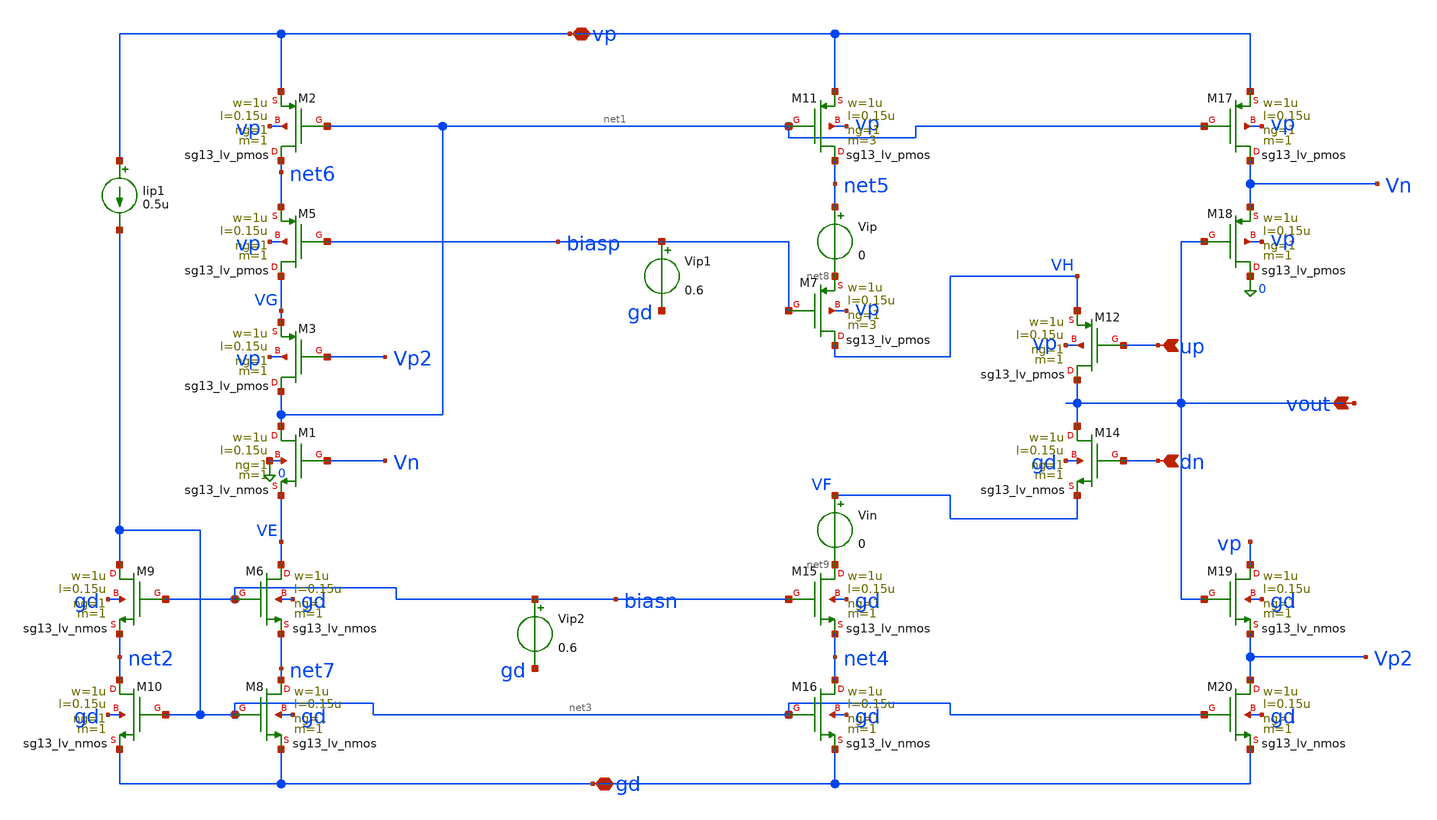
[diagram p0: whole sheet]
** sch_path: schematics/charge_pump/cp_v1_low_curr.sch
**.subckt cp_v1_low_curr up dn vp gd vout
*.ipin up
*.ipin dn
*.iopin vp
*.iopin gd
*.opin vout
XM7 VH biasp net8 vp sg13_lv_pmos w=1u l=0.15u ng=1 m=3 mm_ok=1
XM12 vout up VH vp sg13_lv_pmos w=1u l=0.15u ng=1 m=1 mm_ok=1
XM14 vout dn VF gd sg13_lv_nmos w=1u l=0.15u ng=1 m=1 mm_ok=1
XM15 net9 biasn net4 gd sg13_lv_nmos w=1u l=0.15u ng=1 m=1 mm_ok=1
XM16 net4 net3 gd gd sg13_lv_nmos w=1u l=0.15u ng=1 m=1 mm_ok=1
XM17 Vn net1 vp vp sg13_lv_pmos w=1u l=0.15u ng=1 m=1 mm_ok=1
XM18 0 vout Vn vp sg13_lv_pmos w=1u l=0.15u ng=1 m=1 mm_ok=1
XM19 vp vout Vp2 gd sg13_lv_nmos w=1u l=0.15u ng=1 m=1 mm_ok=1
XM20 Vp2 net3 gd gd sg13_lv_nmos w=1u l=0.15u ng=1 m=1 mm_ok=1
XM1 net1 Vn VE 0 sg13_lv_nmos w=1u l=0.15u ng=1 m=1 mm_ok=1
XM2 net6 net1 vp vp sg13_lv_pmos w=1u l=0.15u ng=1 m=1 mm_ok=1
XM5 VG biasp net6 vp sg13_lv_pmos w=1u l=0.15u ng=1 m=1 mm_ok=1
XM3 net1 Vp2 VG vp sg13_lv_pmos w=1u l=0.15u ng=1 m=1 mm_ok=1
XM6 VE biasn net7 gd sg13_lv_nmos w=1u l=0.15u ng=1 m=1 mm_ok=1
XM8 net7 net3 gd gd sg13_lv_nmos w=1u l=0.15u ng=1 m=1 mm_ok=1
XM9 net3 biasn net2 gd sg13_lv_nmos w=1u l=0.15u ng=1 m=1 mm_ok=1
XM10 net2 net3 gd gd sg13_lv_nmos w=1u l=0.15u ng=1 m=1 mm_ok=1
Vip net5 net8 0
Vin VF net9 0
XM11 net5 net1 vp vp sg13_lv_pmos w=1u l=0.15u ng=1 m=3 mm_ok=1
Iip1 vp net3 0.5u
Vip1 biasp gd 0.6
Vip2 biasn gd 0.6
**.ends
.end
